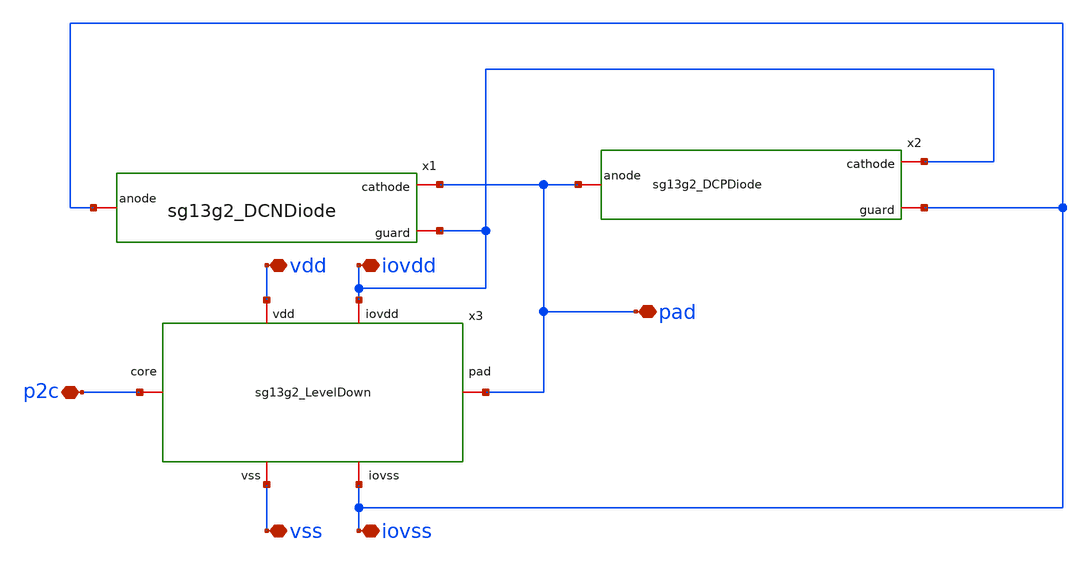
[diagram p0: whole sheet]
** sch_path: ihp-sg13g2/libs.ref/sg13g2_io/xschem/sg13g2_IOPadIn.sch
**.subckt sg13g2_IOPadIn iovdd vdd vss iovss p2c pad
*.iopin iovdd
*.iopin vdd
*.iopin vss
*.iopin iovss
*.iopin p2c
*.iopin pad
x1 pad iovss iovdd sg13g2_DCNDiode
x2 iovdd pad iovss sg13g2_DCPDiode
x3 vdd iovdd p2c pad iovss vss sg13g2_LevelDown
**.ends

* expanding   symbol:  sg13g2_DCNDiode.sym # of pins=3
** sym_path: ihp-sg13g2/libs.ref/sg13g2_io/xschem/sg13g2_DCNDiode.sym
** sch_path: ihp-sg13g2/libs.ref/sg13g2_io/xschem/sg13g2_DCNDiode.sch
.subckt sg13g2_DCNDiode cathode anode guard
*.iopin cathode
*.iopin anode
*.iopin guard
XD1 anode cathode dantenna l=1.26u w=27.78u
XD2 anode cathode dantenna l=1.26u w=27.78u
.ends


* expanding   symbol:  sg13g2_DCPDiode.sym # of pins=3
** sym_path: ihp-sg13g2/libs.ref/sg13g2_io/xschem/sg13g2_DCPDiode.sym
** sch_path: ihp-sg13g2/libs.ref/sg13g2_io/xschem/sg13g2_DCPDiode.sch
.subckt sg13g2_DCPDiode cathode anode guard
*.iopin cathode
*.iopin anode
*.iopin guard
XD1 anode cathode dpantenna l=1.26u w=27.78u
XD2 anode cathode dpantenna l=1.26u w=27.78u
.ends


* expanding   symbol:  sg13g2_LevelDown.sym # of pins=6
** sym_path: ihp-sg13g2/libs.ref/sg13g2_io/xschem/sg13g2_LevelDown.sym
** sch_path: ihp-sg13g2/libs.ref/sg13g2_io/xschem/sg13g2_LevelDown.sch
.subckt sg13g2_LevelDown vdd iovdd core pad iovss vss
*.iopin vdd
*.iopin vss
*.iopin iovdd
*.iopin iovss
*.iopin pad
*.iopin core
XM1 vss net2 net1 vss sg13_hv_nmos w=2.65u l=0.45u ng=1 m=1 mm_ok=1
XM2 net1 net2 vdd vdd sg13_hv_pmos w=4.65u l=0.45u ng=1 m=1 mm_ok=1
XM3 vss net1 core vss sg13_lv_nmos w=2.75u l=0.13u ng=1 m=1 mm_ok=1
XM4 core net1 vdd vdd sg13_lv_pmos w=4.75u l=0.13u ng=1 m=1 mm_ok=1
x1 iovdd pad net2 iovss sg13g2_SecondaryProtection
.ends


* expanding   symbol:  sg13g2_SecondaryProtection.sym # of pins=4
** sym_path: ihp-sg13g2/libs.ref/sg13g2_io/xschem/sg13g2_SecondaryProtection.sym
** sch_path: ihp-sg13g2/libs.ref/sg13g2_io/xschem/sg13g2_SecondaryProtection.sch
.subckt sg13g2_SecondaryProtection iovdd pad core iovss
*.iopin iovdd
*.iopin iovss
*.iopin core
*.iopin pad
XR1 core pad sub! rppd w=1e-6 l=2e-6 m=1 b=0 mm_ok=1
XD1 iovss core dantenna l=3.1u w=0.64u
XD2 core iovdd dpantenna l=0.64u w=4.98u
.ends

.end
